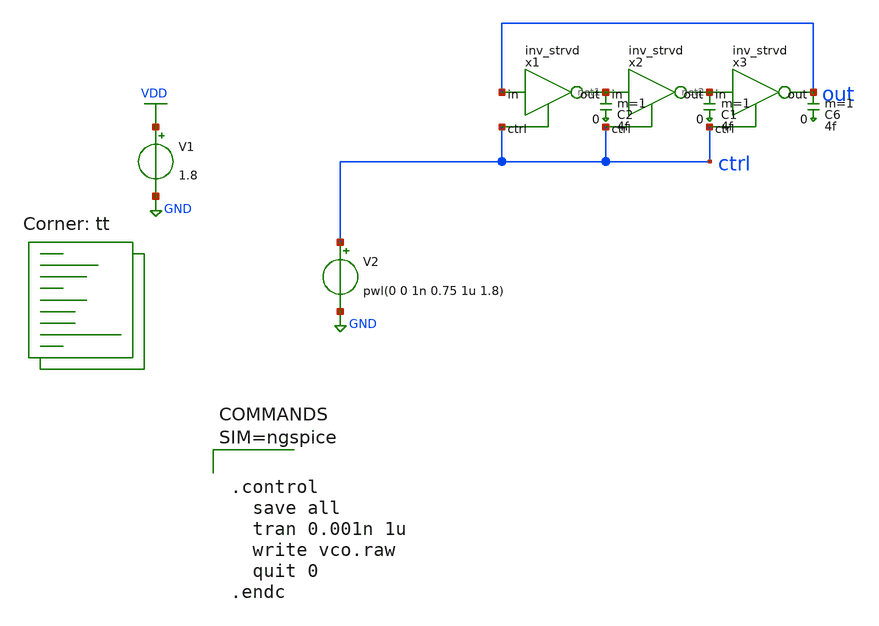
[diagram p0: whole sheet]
** sch_path: tt_um_wulf_8bit_vco/xschem/vco.sch
**.subckt vco
V1 VDD GND 1.8
V2 ctrl GND pwl(0 0 1n 0.75 1u 1.8)
x1 out net1 ctrl VDD GND inv_strvd
x2 net1 net2 ctrl VDD GND inv_strvd
x3 net2 out ctrl VDD GND inv_strvd
C6 out 0 4f m=1
C1 net2 0 4f m=1
C2 net1 0 4f m=1
**** begin user architecture code



.control
  save all
  tran 0.001n 1u
  write vco.raw
  quit 0
.endc



.lib $::SKYWATER_MODELS/sky130.lib.spice tt
**** end user architecture code
**.ends

* expanding   symbol:  lib/inv_strvd.sym # of pins=3
** sym_path: archive/tt_um_wulf_8bit_vco/xschem/lib/inv_strvd.sym
** sch_path: archive/tt_um_wulf_8bit_vco/xschem/lib/inv_strvd.sch
.subckt inv_strvd in out ctrl VDD VSS
*.ipin in
*.ipin ctrl
*.opin out
XM2 out in net1 net1 sky130_fd_pr__nfet_01v8 L=1 W=40 nf=1 ad='int((1 + 1)/2) * 40 / 1 * 0.29' as='int((1 + 2)/2) * 40 / 1 * 0.29'
+ pd='2*int((1 + 1)/2) * (40 / 1 + 0.29)' ps='2*int((1 + 2)/2) * (40 / 1 + 0.29)' nrd='0.29 / 40 ' nrs='0.29 / 40 '
+ sa=0 sb=0 sd=0 mult=1 m=1
XM3 net1 ctrl VSS VSS sky130_fd_pr__nfet_01v8 L=0.15 W=1 nf=1 ad='int((1 + 1)/2) * 1 / 1 * 0.29' as='int((1 + 2)/2) * 1 / 1 * 0.29'
+ pd='2*int((1 + 1)/2) * (1 / 1 + 0.29)' ps='2*int((1 + 2)/2) * (1 / 1 + 0.29)' nrd='0.29 / 1 ' nrs='0.29 / 1 '
+ sa=0 sb=0 sd=0 mult=1 m=1
XM1 out in VDD VDD sky130_fd_pr__pfet_01v8 L=4 W=40 nf=1 ad='int((nf+1)/2) * W/nf * 0.29' as='int((nf+2)/2) * W/nf * 0.29'
+ pd='2*int((nf+1)/2) * (W/nf + 0.29)' ps='2*int((nf+2)/2) * (W/nf + 0.29)' nrd='0.29 / W' nrs='0.29 / W'
+ sa=0 sb=0 sd=0 mult=1 m=1
.ends

.GLOBAL VDD
.GLOBAL GND
.end
